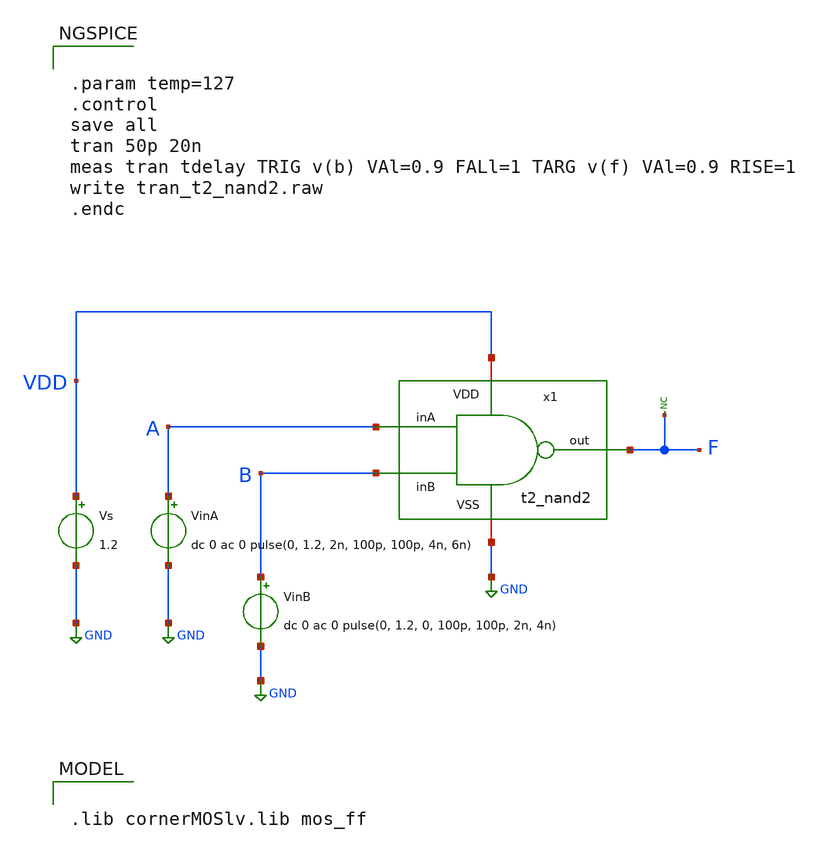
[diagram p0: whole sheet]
** sch_path: Team 2 Design/design_data/xschem/t2_nand2_tb.sch
**.subckt t2_nand2_tb
VinA A GND dc 0 ac 0 pulse(0, 1.2, 2n, 100p, 100p, 4n, 6n)
VinB B GND dc 0 ac 0 pulse(0, 1.2, 0, 100p, 100p, 2n, 4n)
Vs VDD GND 1.2
* noconn F
x1 VDD A B F GND t2_nand2
**** begin user architecture code


.param temp=127
.control
save all
tran 50p 20n
meas tran tdelay TRIG v(b) VAl=0.9 FALl=1 TARG v(f) VAl=0.9 RISE=1
write tran_t2_nand2.raw
.endc



.lib cornerMOSlv.lib mos_ff

**** end user architecture code
**.ends

* expanding   symbol:  t2_nand2.sym # of pins=5
** sym_path: Team 2 Design/design_data/xschem/t2_nand2.sym
** sch_path: Team 2 Design/design_data/xschem/t2_nand2.sch
.subckt t2_nand2 VDD inA inB out VSS
*.iopin VSS
*.ipin inA
*.ipin inB
*.opin out
*.iopin VDD
XM1 out inA VDD VDD sg13_lv_pmos w=0.3u l=0.15u ng=1 m=1 mm_ok=1
XM2 out inB VDD VDD sg13_lv_pmos w=0.3u l=0.13u ng=1 m=1 mm_ok=1
XM3 out inB net1 VSS sg13_lv_nmos w=0.15u l=0.13u ng=1 m=1 mm_ok=1
XM4 net1 inA VSS VSS sg13_lv_nmos w=0.15u l=0.13u ng=1 m=1 mm_ok=1
.ends

.GLOBAL GND
.end
